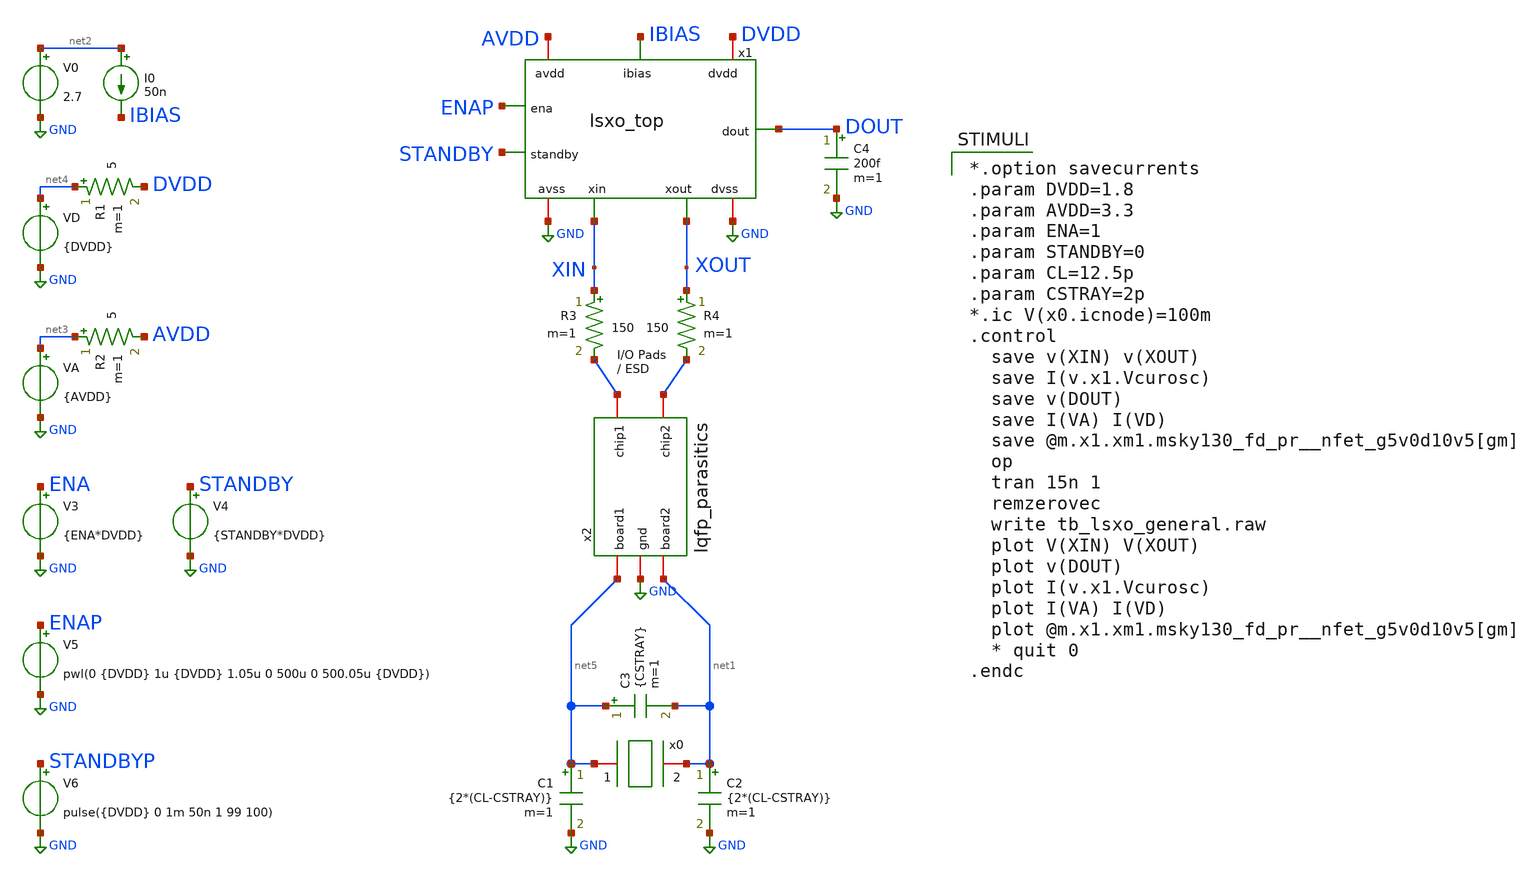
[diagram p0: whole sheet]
** sch_path: xschem/tb_lsxo_general.sch

.lib $::SKYWATER_MODELS/sky130.lib.spice tt
.include $::SKYWATER_STDCELLS/sky130_fd_sc_hd.spice

**.subckt tb_lsxo_general
VD net4 GND {DVDD}
VA net3 GND {AVDD}
C1 net5 GND {2*(CL-CSTRAY)} m=1
C2 net1 GND {2*(CL-CSTRAY)} m=1
C3 net5 net1 {CSTRAY} m=1
I0 net2 IBIAS 50n
C4 DOUT GND 200f m=1
V0 net2 GND 2.7
V3 ENA GND {ENA*DVDD}
V4 STANDBY GND {STANDBY*DVDD}
x1 AVDD GND DVDD GND IBIAS ENAP STANDBY DOUT XIN XOUT lsxo_top
V5 ENAP GND pwl(0 {DVDD} 1u {DVDD} 1.05u 0 500u 0 500.05u {DVDD})
V6 STANDBYP GND pulse({DVDD} 0 1m 50n 1 99 100)
R1 net4 DVDD 5 m=1
R2 net3 AVDD 5 m=1
R3 XIN net6 150 m=1
R4 XOUT net7 150 m=1
x2 net7 net6 GND net5 net1 lqfp_parasitics
x0 net5 net1 xtal_iqd_125_1
**** begin user architecture code

*.option savecurrents
.param DVDD=1.8
.param AVDD=3.3
.param ENA=1
.param STANDBY=0
.param CL=12.5p
.param CSTRAY=2p
*.ic V(x0.icnode)=100m
.control
  save v(XIN) v(XOUT)
  save I(v.x1.Vcurosc)
  save v(DOUT)
  save I(VA) I(VD)
  save @m.x1.xm1.msky130_fd_pr__nfet_g5v0d10v5[gm]
  op
  tran 15n 1
  remzerovec
  write tb_lsxo_general.raw
  plot V(XIN) V(XOUT)
  plot v(DOUT)
  plot I(v.x1.Vcurosc)
  plot I(VA) I(VD)
  plot @m.x1.xm1.msky130_fd_pr__nfet_g5v0d10v5[gm]
  * quit 0
.endc

**** end user architecture code
**.ends
.GLOBAL GND
.end
